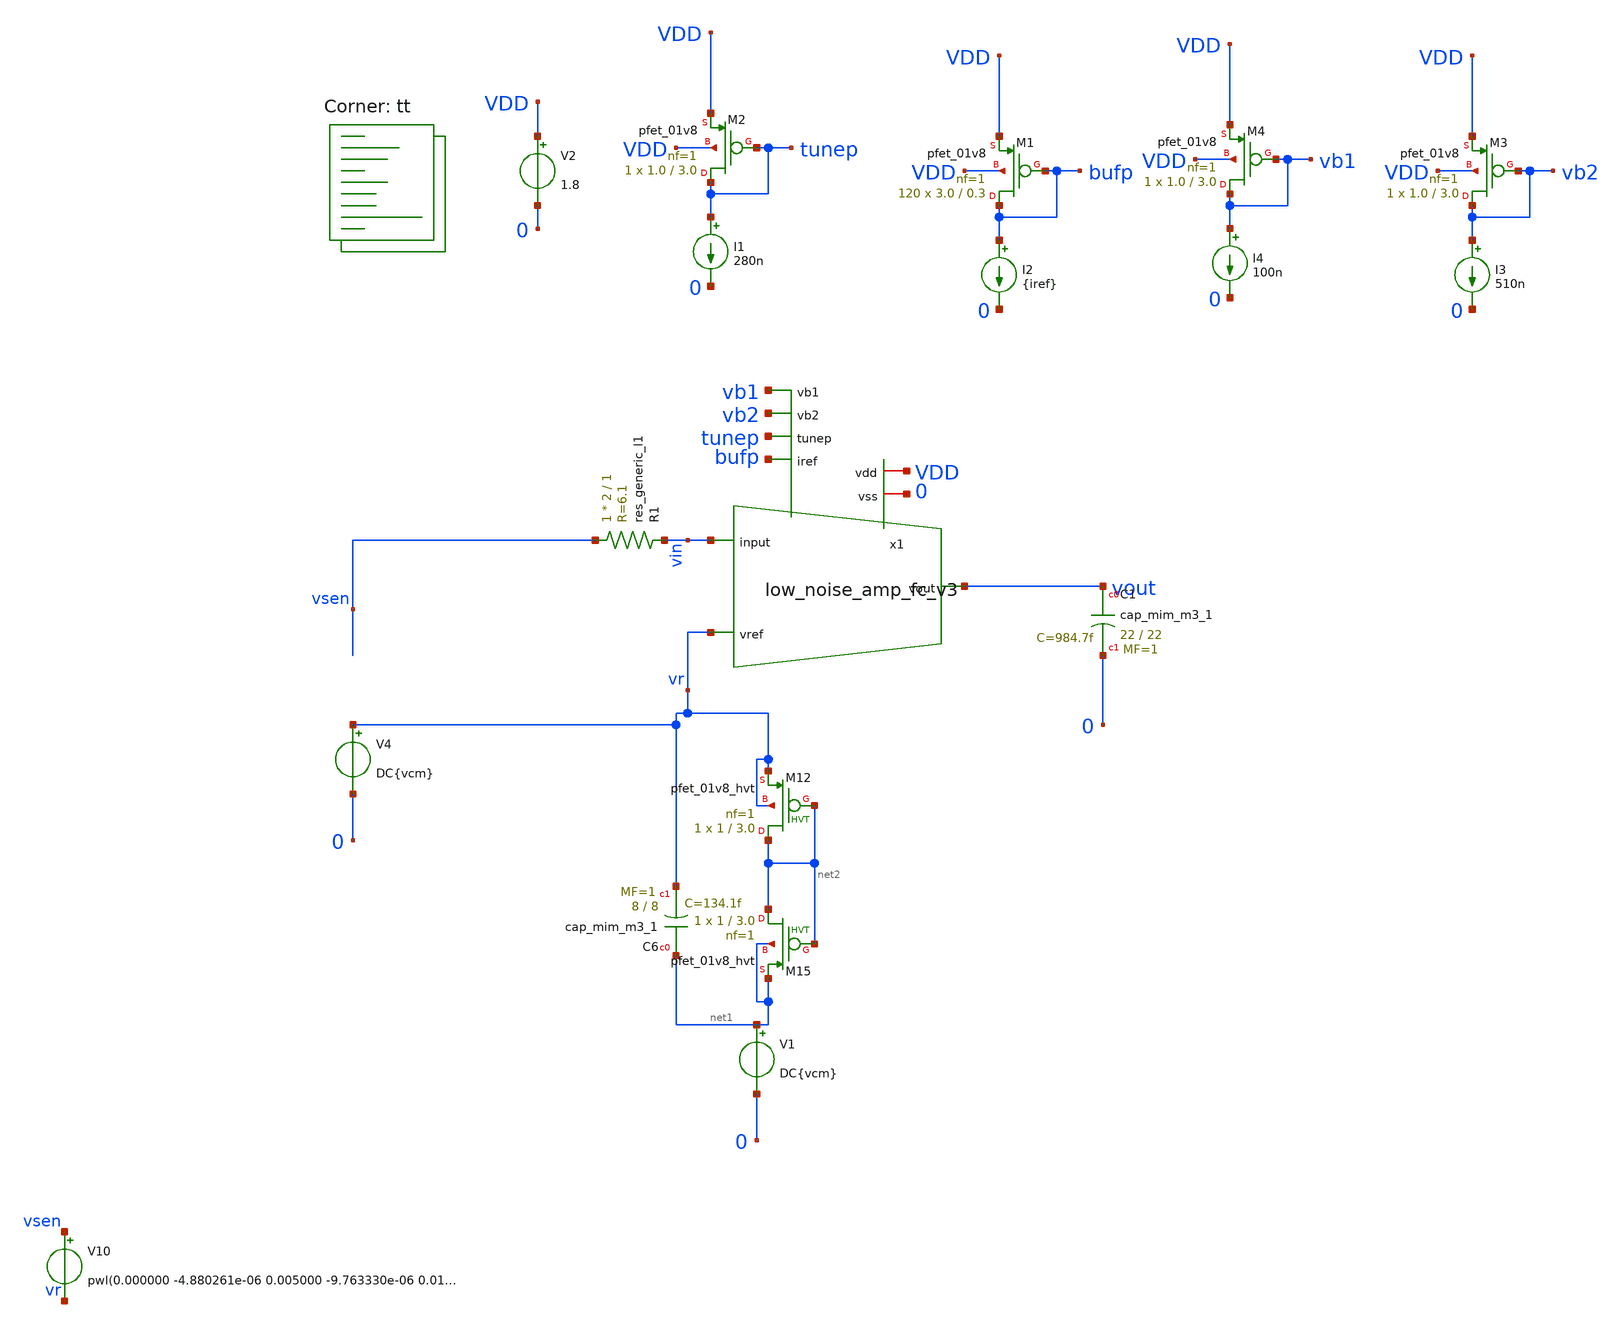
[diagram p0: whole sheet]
** sch_path: design/xschem/LNA_singletrace.sch
**.subckt LNA_singletrace
V2 VDD 0 1.8
XC1 vout 0 sky130_fd_pr__cap_mim_m3_1 W=22 L=22 MF=1 m=1
XM1 bufp bufp VDD VDD sky130_fd_pr__pfet_01v8 L=0.3 W=3.0 nf=1 ad='W * 0.29' as='W * 0.29' pd='2 * (W + 0.29)'
+ ps='2 * (W + 0.29)' nrd='0.29 / W' nrs='0.29 / W' sa=0 sb=0 sd=0 mult=120 m=120
I2 bufp 0 {iref}
R1 vsen vin sky130_fd_pr__res_generic_l1 W=2 L=1 m=1
XM2 tunep tunep VDD VDD sky130_fd_pr__pfet_01v8 L=3.0 W=1.0 nf=1 ad='W * 0.29' as='W * 0.29' pd='2 * (W + 0.29)'
+ ps='2 * (W + 0.29)' nrd='0.29 / W' nrs='0.29 / W' sa=0 sb=0 sd=0 mult=1 m=1
I1 tunep 0 280n
x1 0 vb1 vb2 vout vin VDD bufp vr tunep low_noise_amp_fc_v3
I3 vb2 0 510n
XM4 vb1 vb1 VDD VDD sky130_fd_pr__pfet_01v8 L=3.0 W=1.0 nf=1 ad='W * 0.29' as='W * 0.29' pd='2 * (W + 0.29)'
+ ps='2 * (W + 0.29)' nrd='0.29 / W' nrs='0.29 / W' sa=0 sb=0 sd=0 mult=1 m=1
I4 vb1 0 100n
XM3 vb2 vb2 VDD VDD sky130_fd_pr__pfet_01v8 L=3.0 W=1.0 nf=1 ad='W * 0.29' as='W * 0.29' pd='2 * (W + 0.29)'
+ ps='2 * (W + 0.29)' nrd='0.29 / W' nrs='0.29 / W' sa=0 sb=0 sd=0 mult=1 m=1
V1 net1 0 DC{vcm}
XC6 net1 vr sky130_fd_pr__cap_mim_m3_1 W=8 L=8 MF=1 m=1
XM12 net2 net2 vr vr sky130_fd_pr__pfet_01v8_hvt L=3.0 W=1 nf=1 ad='int((nf+1)/2) * W/nf * 0.29' as='int((nf+2)/2) * W/nf * 0.29'
+ pd='2*int((nf+1)/2) * (W/nf + 0.29)' ps='2*int((nf+2)/2) * (W/nf + 0.29)' nrd='0.29 / W' nrs='0.29 / W'
+ sa=0 sb=0 sd=0 mult=1 m=1
XM15 net2 net2 net1 net1 sky130_fd_pr__pfet_01v8_hvt L=3.0 W=1 nf=1 ad='int((nf+1)/2) * W/nf * 0.29'
+ as='int((nf+2)/2) * W/nf * 0.29' pd='2*int((nf+1)/2) * (W/nf + 0.29)' ps='2*int((nf+2)/2) * (W/nf + 0.29)'
+ nrd='0.29 / W' nrs='0.29 / W' sa=0 sb=0 sd=0 mult=1 m=1
V4 vr 0 DC{vcm}
V10 vsen vr pwl(0.000000 -4.880261e-06 0.005000 -9.763330e-06 0.010000 9.908184e-06 0.015000
+ 5.515938e-06 0.020000 2.244229e-06 0.025000 3.660483e-06 0.030000 2.868774e-06 0.035000 -2.551013e-06 0.040000
+ 9.030370e-06 0.045000 -5.404867e-06 0.050000 5.725756e-07 0.055000 1.380211e-06 0.060000 4.043288e-07 0.065000
+ -3.140963e-06 0.070000 2.905914e-06 0.075000 -7.295456e-06 0.080000 -7.757795e-06 0.085000 -7.080568e-07 0.090000
+ -5.557280e-06 0.095000 -7.755975e-06 0.100000 -7.066066e-06 0.105000 5.620001e-06 0.110000 -3.448490e-06 0.115000
+ -1.676242e-06 0.120000 -4.166483e-06 0.125000 -7.502806e-06 0.130000 -4.546691e-06 0.135000 -1.982050e-06
+ 0.140000 8.487507e-06 0.145000 -9.397028e-06 0.150000 -1.376018e-06 0.155000 3.975320e-06 0.160000
+ -9.726614e-06 0.165000 1.398255e-06 0.170000 -6.629112e-06 0.175000 4.710097e-06 0.180000 -6.078078e-06 0.185000
+ -7.633672e-06 0.190000 -8.445954e-07 0.195000 3.923504e-06 0.200000 -4.903990e-07 0.205000 -8.405587e-06 0.210000
+ -2.587027e-06 0.215000 5.028946e-06 0.220000 7.502805e-06 0.225000 -5.321348e-06 0.230000 -3.741690e-06 0.235000
+ -2.872865e-06 0.240000 3.394512e-06 0.245000 1.637796e-06 0.250000 0.000000e+00 0.255000 1.179841e-07 0.260000
+ -1.386146e-05 0.265000 -6.121421e-05 0.270000 -6.031904e-05 0.275000 -7.987478e-05 0.280000 -7.494862e-05
+ 0.285000 -8.306139e-05 0.290000 -8.587100e-05 0.295000 -1.078314e-04 0.300000 -1.109067e-04 0.305000
+ -9.854137e-05 0.310000 -1.054329e-04 0.315000 -1.124799e-04 0.320000 -1.133720e-04 0.325000 -1.215143e-04
+ 0.330000 -1.088613e-04 0.335000 -1.291208e-04 0.340000 -1.224607e-04 0.345000 -1.250127e-04 0.350000
+ -1.142592e-04 0.355000 -1.136365e-04 0.360000 -1.023870e-04 0.365000 -9.565126e-05 0.370000 -1.018684e-04
+ 0.375000 -1.028745e-04 0.380000 -9.461381e-05 0.385000 -8.532380e-05 0.390000 -1.050614e-04 0.395000
+ -8.914857e-05 0.400000 -8.957664e-05 0.405000 -9.355703e-05 0.410000 -1.144333e-04 0.415000 -1.022252e-04
+ 0.420000 -1.065815e-04 0.425000 -8.519650e-05 0.430000 -9.588891e-05 0.435000 -1.081031e-04 0.440000
+ -1.194637e-04 0.445000 -1.249378e-04 0.450000 -1.190131e-04 0.455000 -1.145037e-04 0.460000 -1.128526e-04
+ 0.465000 -1.125965e-04 0.470000 -1.044394e-04 0.475000 -9.730458e-05 0.480000 -8.362232e-05 0.485000
+ -7.017312e-05 0.490000 -8.687710e-05 0.495000 -9.978706e-05 0.500000 -9.273670e-05 0.505000 -8.400265e-05
+ 0.510000 -9.406079e-05 0.515000 -8.191100e-05 0.520000 -7.756449e-05 0.525000 -7.213289e-05 0.530000
+ -8.099025e-05 0.535000 -9.722732e-05 0.540000 -9.234096e-05 0.545000 -1.001006e-04 0.550000 -9.318990e-05
+ 0.555000 -7.326445e-05 0.560000 -6.698518e-05 0.565000 -4.306706e-06 0.570000 -7.399993e-06 0.575000
+ -8.240923e-06 0.580000 7.767451e-06 0.585000 -6.449711e-06 0.590000 1.745394e-06 0.595000 2.476606e-06 0.600000
+ -9.753836e-06 0.605000 -6.890178e-06 0.610000 5.842249e-06 0.615000 5.858399e-06 0.620000 5.793911e-06 0.625000
+ 2.631263e-06 0.630000 8.808085e-06 0.635000 -6.835229e-07 0.640000 7.528215e-06 0.645000 -6.975091e-06 0.650000
+ 9.384998e-06 0.655000 7.274380e-07 0.660000 -2.200938e-06 0.665000 -1.103119e-06 0.670000 2.115765e-06 0.675000
+ 2.108737e-06 0.680000 4.604041e-06 0.685000 2.869609e-06 0.690000 -2.308084e-06 0.695000 8.005138e-06 0.700000
+ 7.537152e-06 0.705000 -3.589705e-06 0.710000 -1.911070e-06 0.715000 6.263005e-06 0.720000 -2.449097e-06 0.725000
+ 2.194615e-06 0.730000 -9.217524e-06 0.735000 4.314929e-07 0.740000 -3.037816e-06 0.745000 5.133013e-06 0.750000
+ -4.905053e-06 0.755000 4.598050e-07 0.760000 1.484264e-06 0.765000 -4.346510e-06 0.770000 -9.093675e-07 0.775000
+ 6.163051e-06 0.780000 -4.949176e-07 0.785000 -3.042939e-06 0.790000 9.907000e-06 0.795000 -4.950915e-07 0.800000
+ 8.645162e-06 0.805000 5.780608e-06 0.810000 5.381109e-07 0.815000 6.857290e-06)
**** begin user architecture code
.lib $::SKYWATER_MODELS/sky130.lib.spice tt



* ngspice commands



* Circuit Parameters
*.param iref1 = 200u
.param iref = 6u
.param vdd  = 1.8
.param vss  = 0.0
.param vcm  = 0.8
.param vac  = 5u
.options TEMP = 35.0


* OP Parameters & Singals to save
.save all

  @M.X1.XM2.msky130_fd_pr__pfet_01v8[id] @M.X1.XM2.msky130_fd_pr__pfet_01v8[vth]
+ @M.X1.XM2.msky130_fd_pr__pfet_01v8[vgs] @M.X1.XM2.msky130_fd_pr__pfet_01v8[vds] @M.X1.XM2.msky130_fd_pr__pfet_01v8[vdsat]
+ @M.X1.XM2.msky130_fd_pr__pfet_01v8[gm] @M.X1.XM2.msky130_fd_pr__pfet_01v8[gds] @M.X1.XM2.msky130_fd_pr__pfet_01v8[cgs]
+  @M.X1.XM1.msky130_fd_pr__pfet_01v8[id] @M.X1.XM1.msky130_fd_pr__pfet_01v8[vth] @M.X1.XM1.msky130_fd_pr__pfet_01v8[vgs]
+ @M.X1.XM1.msky130_fd_pr__pfet_01v8[vds] @M.X1.XM1.msky130_fd_pr__pfet_01v8[vdsat] @M.X1.XM1.msky130_fd_pr__pfet_01v8[gm]
+ @M.X1.XM1.msky130_fd_pr__pfet_01v8[gds]  @M.X1.XM5.msky130_fd_pr__pfet_01v8[id] @M.X1.XM5.msky130_fd_pr__pfet_01v8[vth]
+ @M.X1.XM5.msky130_fd_pr__pfet_01v8[vgs] @M.X1.XM5.msky130_fd_pr__pfet_01v8[vds] @M.X1.XM5.msky130_fd_pr__pfet_01v8[vdsat]
+ @M.X1.XM5.msky130_fd_pr__pfet_01v8[gm] @M.X1.XM5.msky130_fd_pr__pfet_01v8[gds]

  @M.X1.XM3.msky130_fd_pr__nfet_01v8[id] @M.X1.XM3.msky130_fd_pr__nfet_01v8[vth]
+ @M.X1.XM3.msky130_fd_pr__nfet_01v8[vgs] @M.X1.XM3.msky130_fd_pr__nfet_01v8[vds] @M.X1.XM3.msky130_fd_pr__nfet_01v8[vdsat]
+ @M.X1.XM3.msky130_fd_pr__nfet_01v8[gm] @M.X1.XM3.msky130_fd_pr__nfet_01v8[gds]  @M.X1.XM6.msky130_fd_pr__nfet_01v8[id]
+ @M.X1.XM6.msky130_fd_pr__nfet_01v8[vth] @M.X1.XM6.msky130_fd_pr__nfet_01v8[vgs] @M.X1.XM6.msky130_fd_pr__nfet_01v8[vds]
+ @M.X1.XM6.msky130_fd_pr__nfet_01v8[vdsat] @M.X1.XM6.msky130_fd_pr__nfet_01v8[gm] @M.X1.XM6.msky130_fd_pr__nfet_01v8[gds]
+  @M.X1.XM4.msky130_fd_pr__nfet_01v8[id] @M.X1.XM4.msky130_fd_pr__nfet_01v8[vth] @M.X1.XM4.msky130_fd_pr__nfet_01v8[vgs]
+ @M.X1.XM4.msky130_fd_pr__nfet_01v8[vds] @M.X1.XM4.msky130_fd_pr__nfet_01v8[vdsat] @M.X1.XM4.msky130_fd_pr__nfet_01v8[gm]
+ @M.X1.XM4.msky130_fd_pr__nfet_01v8[gds]  @M.X1.XM9.msky130_fd_pr__nfet_01v8[id] @M.X1.XM9.msky130_fd_pr__nfet_01v8[vth]
+ @M.X1.XM9.msky130_fd_pr__nfet_01v8[vgs] @M.X1.XM9.msky130_fd_pr__nfet_01v8[vds] @M.X1.XM9.msky130_fd_pr__nfet_01v8[vdsat]
+ @M.X1.XM9.msky130_fd_pr__nfet_01v8[gm] @M.X1.XM9.msky130_fd_pr__nfet_01v8[gds]
  @M.X1.XM10.msky130_fd_pr__nfet_01v8[id] @M.X1.XM10.msky130_fd_pr__nfet_01v8[vth]
+ @M.X1.XM10.msky130_fd_pr__nfet_01v8[vgs] @M.X1.XM10.msky130_fd_pr__nfet_01v8[vds] @M.X1.XM10.msky130_fd_pr__nfet_01v8[vdsat]
+ @M.X1.XM10.msky130_fd_pr__nfet_01v8[gm] @M.X1.XM10.msky130_fd_pr__nfet_01v8[gds]  @M.X1.XM15.msky130_fd_pr__nfet_01v8[id]
+ @M.X1.XM15.msky130_fd_pr__nfet_01v8[vth] @M.X1.XM15.msky130_fd_pr__nfet_01v8[vgs] @M.X1.XM15.msky130_fd_pr__nfet_01v8[vds]
+ @M.X1.XM15.msky130_fd_pr__nfet_01v8[vdsat] @M.X1.XM15.msky130_fd_pr__nfet_01v8[gm] @M.X1.XM15.msky130_fd_pr__nfet_01v8[gds]
+  @M.X1.XM12.msky130_fd_pr__nfet_01v8[id] @M.X1.XM12.msky130_fd_pr__nfet_01v8[vth] @M.X1.XM12.msky130_fd_pr__nfet_01v8[vgs]
+ @M.X1.XM12.msky130_fd_pr__nfet_01v8[vds] @M.X1.XM12.msky130_fd_pr__nfet_01v8[vdsat] @M.X1.XM12.msky130_fd_pr__nfet_01v8[gm]
+ @M.X1.XM12.msky130_fd_pr__nfet_01v8[gds]  @M.X1.XM7.msky130_fd_pr__nfet_01v8[id] @M.X1.XM7.msky130_fd_pr__nfet_01v8[vth]
+ @M.X1.XM7.msky130_fd_pr__nfet_01v8[vgs] @M.X1.XM7.msky130_fd_pr__nfet_01v8[vds] @M.X1.XM7.msky130_fd_pr__nfet_01v8[vdsat]
+ @M.X1.XM7.msky130_fd_pr__nfet_01v8[gm] @M.X1.XM7.msky130_fd_pr__nfet_01v8[gds]
  @M.X1.XM16.msky130_fd_pr__pfet_01v8[id] @M.X1.XM16.msky130_fd_pr__pfet_01v8[vth]
+ @M.X1.XM16.msky130_fd_pr__pfet_01v8[vgs] @M.X1.XM16.msky130_fd_pr__pfet_01v8[vds] @M.X1.XM16.msky130_fd_pr__pfet_01v8[vdsat]
+ @M.X1.XM16.msky130_fd_pr__pfet_01v8[gm] @M.X1.XM16.msky130_fd_pr__pfet_01v8[gds]  @M.X1.XM27.msky130_fd_pr__pfet_01v8[id]
+ @M.X1.XM27.msky130_fd_pr__pfet_01v8[vth] @M.X1.XM27.msky130_fd_pr__pfet_01v8[vgs] @M.X1.XM27.msky130_fd_pr__pfet_01v8[vds]
+ @M.X1.XM27.msky130_fd_pr__pfet_01v8[vdsat] @M.X1.XM27.msky130_fd_pr__pfet_01v8[gm] @M.X1.XM27.msky130_fd_pr__pfet_01v8[gds]
+  @M.X1.XM17.msky130_fd_pr__pfet_01v8[id] @M.X1.XM17.msky130_fd_pr__pfet_01v8[vth] @M.X1.XM17.msky130_fd_pr__pfet_01v8[vgs]
+ @M.X1.XM17.msky130_fd_pr__pfet_01v8[vds] @M.X1.XM17.msky130_fd_pr__pfet_01v8[vdsat] @M.X1.XM17.msky130_fd_pr__pfet_01v8[gm]
+ @M.X1.XM17.msky130_fd_pr__pfet_01v8[gds]  @M.X1.XM24.msky130_fd_pr__pfet_01v8[id] @M.X1.XM24.msky130_fd_pr__pfet_01v8[vth]
+ @M.X1.XM24.msky130_fd_pr__pfet_01v8[vgs] @M.X1.XM24.msky130_fd_pr__pfet_01v8[vds] @M.X1.XM24.msky130_fd_pr__pfet_01v8[vdsat]
+ @M.X1.XM24.msky130_fd_pr__pfet_01v8[gm] @M.X1.XM24.msky130_fd_pr__pfet_01v8[gds]  @M.X1.XM25.msky130_fd_pr__pfet_01v8[id]
+ @M.X1.XM25.msky130_fd_pr__pfet_01v8[vth] @M.X1.XM25.msky130_fd_pr__pfet_01v8[vgs] @M.X1.XM25.msky130_fd_pr__pfet_01v8[vds]
+ @M.X1.XM25.msky130_fd_pr__pfet_01v8[vdsat] @M.X1.XM25.msky130_fd_pr__pfet_01v8[gm] @M.X1.XM25.msky130_fd_pr__pfet_01v8[gds]
+  @M.X1.XM26.msky130_fd_pr__pfet_01v8[id] @M.X1.XM26.msky130_fd_pr__pfet_01v8[vth] @M.X1.XM26.msky130_fd_pr__pfet_01v8[vgs]
+ @M.X1.XM26.msky130_fd_pr__pfet_01v8[vds] @M.X1.XM26.msky130_fd_pr__pfet_01v8[vdsat] @M.X1.XM26.msky130_fd_pr__pfet_01v8[gm]
+ @M.X1.XM26.msky130_fd_pr__pfet_01v8[gds]



*Simulations
.control

  *set filetype=ascii
  *load /tmp/pwl_lna_input.txt


  reset
  tran 1u 0.8s
  setplot tran1
  plot v(vsen) v(vout)
  write opamp_closeloop_tran1.raw vsen vout

  reset
  op
  setplot op1
  print vout
  write opamp_closeloop_op1_v3_fctoday.raw

.endc

.end



**** end user architecture code
**.ends

* expanding   symbol:  low_noise_amp_fc_v3.sym # of pins=10
** sym_path: design/xschem/low_noise_amp_fc_v3.sym
** sch_path: design/xschem/low_noise_amp_fc_v3.sch
.subckt low_noise_amp_fc_v3 vss vb1 vb2 vout input vdd iref vref tunep
*.iopin vdd
*.iopin vss
*.ipin vref
*.ipin iref
*.ipin input
*.opin vout
*.ipin tunep
*.ipin vb1
*.ipin vb2
XM1 vy vin vp vdd sky130_fd_pr__pfet_01v8 L=2.0 W=4.0 nf=1 ad='W * 0.29' as='W * 0.29' pd='2 * (W + 0.29)'
+ ps='2 * (W + 0.29)' nrd='0.29 / W' nrs='0.29 / W' sa=0 sb=0 sd=0 mult=300 m=300
XM2 vx vref vp vdd sky130_fd_pr__pfet_01v8 L=2.0 W=4.0 nf=1 ad='W * 0.29' as='W * 0.29' pd='2 * (W + 0.29)'
+ ps='2 * (W + 0.29)' nrd='0.29 / W' nrs='0.29 / W' sa=0 sb=0 sd=0 mult=300 m=300
XM5 vp iref vdd vdd sky130_fd_pr__pfet_01v8 L=0.3 W=3 nf=1 ad='W * 0.29' as='W * 0.29' pd='2 * (W + 0.29)'
+ ps='2 * (W + 0.29)' nrd='0.29 / W' nrs='0.29 / W' sa=0 sb=0 sd=0 mult=120 m=120
XC6 vin vout sky130_fd_pr__cap_mim_m3_1 W=5 L=5 MF=1 m=1
XM6 vx net1 net2 vss sky130_fd_pr__nfet_01v8 L=20.0 W=8.0 nf=1 ad='W * 0.29' as='W * 0.29' pd='2 * (W + 0.29)'
+ ps='2 * (W + 0.29)' nrd='0.29 / W' nrs='0.29 / W' sa=0 sb=0 sd=0 mult=1 m=1
XM9 vy net1 net3 vss sky130_fd_pr__nfet_01v8 L=20.0 W=8.0 nf=1 ad='W * 0.29' as='W * 0.29' pd='2 * (W + 0.29)'
+ ps='2 * (W + 0.29)' nrd='0.29 / W' nrs='0.29 / W' sa=0 sb=0 sd=0 mult=1 m=1
XM10 net1 net4 vx vss sky130_fd_pr__nfet_01v8 L=1.0 W=10.0 nf=1 ad='W * 0.29' as='W * 0.29' pd='2 * (W + 0.29)'
+ ps='2 * (W + 0.29)' nrd='0.29 / W' nrs='0.29 / W' sa=0 sb=0 sd=0 mult=1 m=1
XM12 vout net7 vy vss sky130_fd_pr__nfet_01v8 L=1.0 W=10.0 nf=1 ad='W * 0.29' as='W * 0.29' pd='2 * (W + 0.29)'
+ ps='2 * (W + 0.29)' nrd='0.29 / W' nrs='0.29 / W' sa=0 sb=0 sd=0 mult=1 m=1
XM15 net4 vx vss vss sky130_fd_pr__nfet_01v8 L=2.0 W=15.0 nf=1 ad='W * 0.29' as='W * 0.29' pd='2 * (W + 0.29)'
+ ps='2 * (W + 0.29)' nrd='0.29 / W' nrs='0.29 / W' sa=0 sb=0 sd=0 mult=1 m=1
XM16 net4 tunep vdd vdd sky130_fd_pr__pfet_01v8 L=3.0 W=1.0 nf=1 ad='W * 0.29' as='W * 0.29' pd='2 * (W + 0.29)'
+ ps='2 * (W + 0.29)' nrd='0.29 / W' nrs='0.29 / W' sa=0 sb=0 sd=0 mult=1 m=1
XM17 net1 vb2 net5 vdd sky130_fd_pr__pfet_01v8 L=3.0 W=1.0 nf=1 ad='W * 0.29' as='W * 0.29' pd='2 * (W + 0.29)'
+ ps='2 * (W + 0.29)' nrd='0.29 / W' nrs='0.29 / W' sa=0 sb=0 sd=0 mult=1 m=1
XM24 vout vb2 net6 vdd sky130_fd_pr__pfet_01v8 L=3.0 W=1.0 nf=1 ad='W * 0.29' as='W * 0.29' pd='2 * (W + 0.29)'
+ ps='2 * (W + 0.29)' nrd='0.29 / W' nrs='0.29 / W' sa=0 sb=0 sd=0 mult=1 m=1
XM25 net5 vb1 vdd vdd sky130_fd_pr__pfet_01v8 L=3.0 W=1.0 nf=1 ad='W * 0.29' as='W * 0.29' pd='2 * (W + 0.29)'
+ ps='2 * (W + 0.29)' nrd='0.29 / W' nrs='0.29 / W' sa=0 sb=0 sd=0 mult=1 m=1
XM26 net6 vb1 vdd vdd sky130_fd_pr__pfet_01v8 L=3.0 W=1.0 nf=1 ad='W * 0.29' as='W * 0.29' pd='2 * (W + 0.29)'
+ ps='2 * (W + 0.29)' nrd='0.29 / W' nrs='0.29 / W' sa=0 sb=0 sd=0 mult=1 m=1
XM7 net7 vy vss vss sky130_fd_pr__nfet_01v8 L=2.0 W=15.0 nf=1 ad='W * 0.29' as='W * 0.29' pd='2 * (W + 0.29)'
+ ps='2 * (W + 0.29)' nrd='0.29 / W' nrs='0.29 / W' sa=0 sb=0 sd=0 mult=1 m=1
XM27 net7 tunep vdd vdd sky130_fd_pr__pfet_01v8 L=3.0 W=1.0 nf=1 ad='W * 0.29' as='W * 0.29' pd='2 * (W + 0.29)'
+ ps='2 * (W + 0.29)' nrd='0.29 / W' nrs='0.29 / W' sa=0 sb=0 sd=0 mult=1.0 m=1.0
XM36 vres vres vin vin sky130_fd_pr__pfet_01v8_hvt L=3.0 W=1.0 nf=1 ad='int((nf+1)/2) * W/nf * 0.29'
+ as='int((nf+2)/2) * W/nf * 0.29' pd='2*int((nf+1)/2) * (W/nf + 0.29)' ps='2*int((nf+2)/2) * (W/nf + 0.29)'
+ nrd='0.29 / W' nrs='0.29 / W' sa=0 sb=0 sd=0 mult=1 m=1
XM37 vres vres vout vout sky130_fd_pr__pfet_01v8_hvt L=3.0 W=1.0 nf=1 ad='int((nf+1)/2) * W/nf * 0.29'
+ as='int((nf+2)/2) * W/nf * 0.29' pd='2*int((nf+1)/2) * (W/nf + 0.29)' ps='2*int((nf+2)/2) * (W/nf + 0.29)'
+ nrd='0.29 / W' nrs='0.29 / W' sa=0 sb=0 sd=0 mult=1 m=1
XM3 net2 net1 vss vss sky130_fd_pr__nfet_01v8 L=20.0 W=8.0 nf=1 ad='W * 0.29' as='W * 0.29' pd='2 * (W + 0.29)'
+ ps='2 * (W + 0.29)' nrd='0.29 / W' nrs='0.29 / W' sa=0 sb=0 sd=0 mult=1 m=1
XM4 net3 net1 vss vss sky130_fd_pr__nfet_01v8 L=20.0 W=8.0 nf=1 ad='W * 0.29' as='W * 0.29' pd='2 * (W + 0.29)'
+ ps='2 * (W + 0.29)' nrd='0.29 / W' nrs='0.29 / W' sa=0 sb=0 sd=0 mult=1 m=1
XC1 vin input sky130_fd_pr__cap_mim_m3_1 W=132 L=70 MF=1 m=1
.ends

.end
